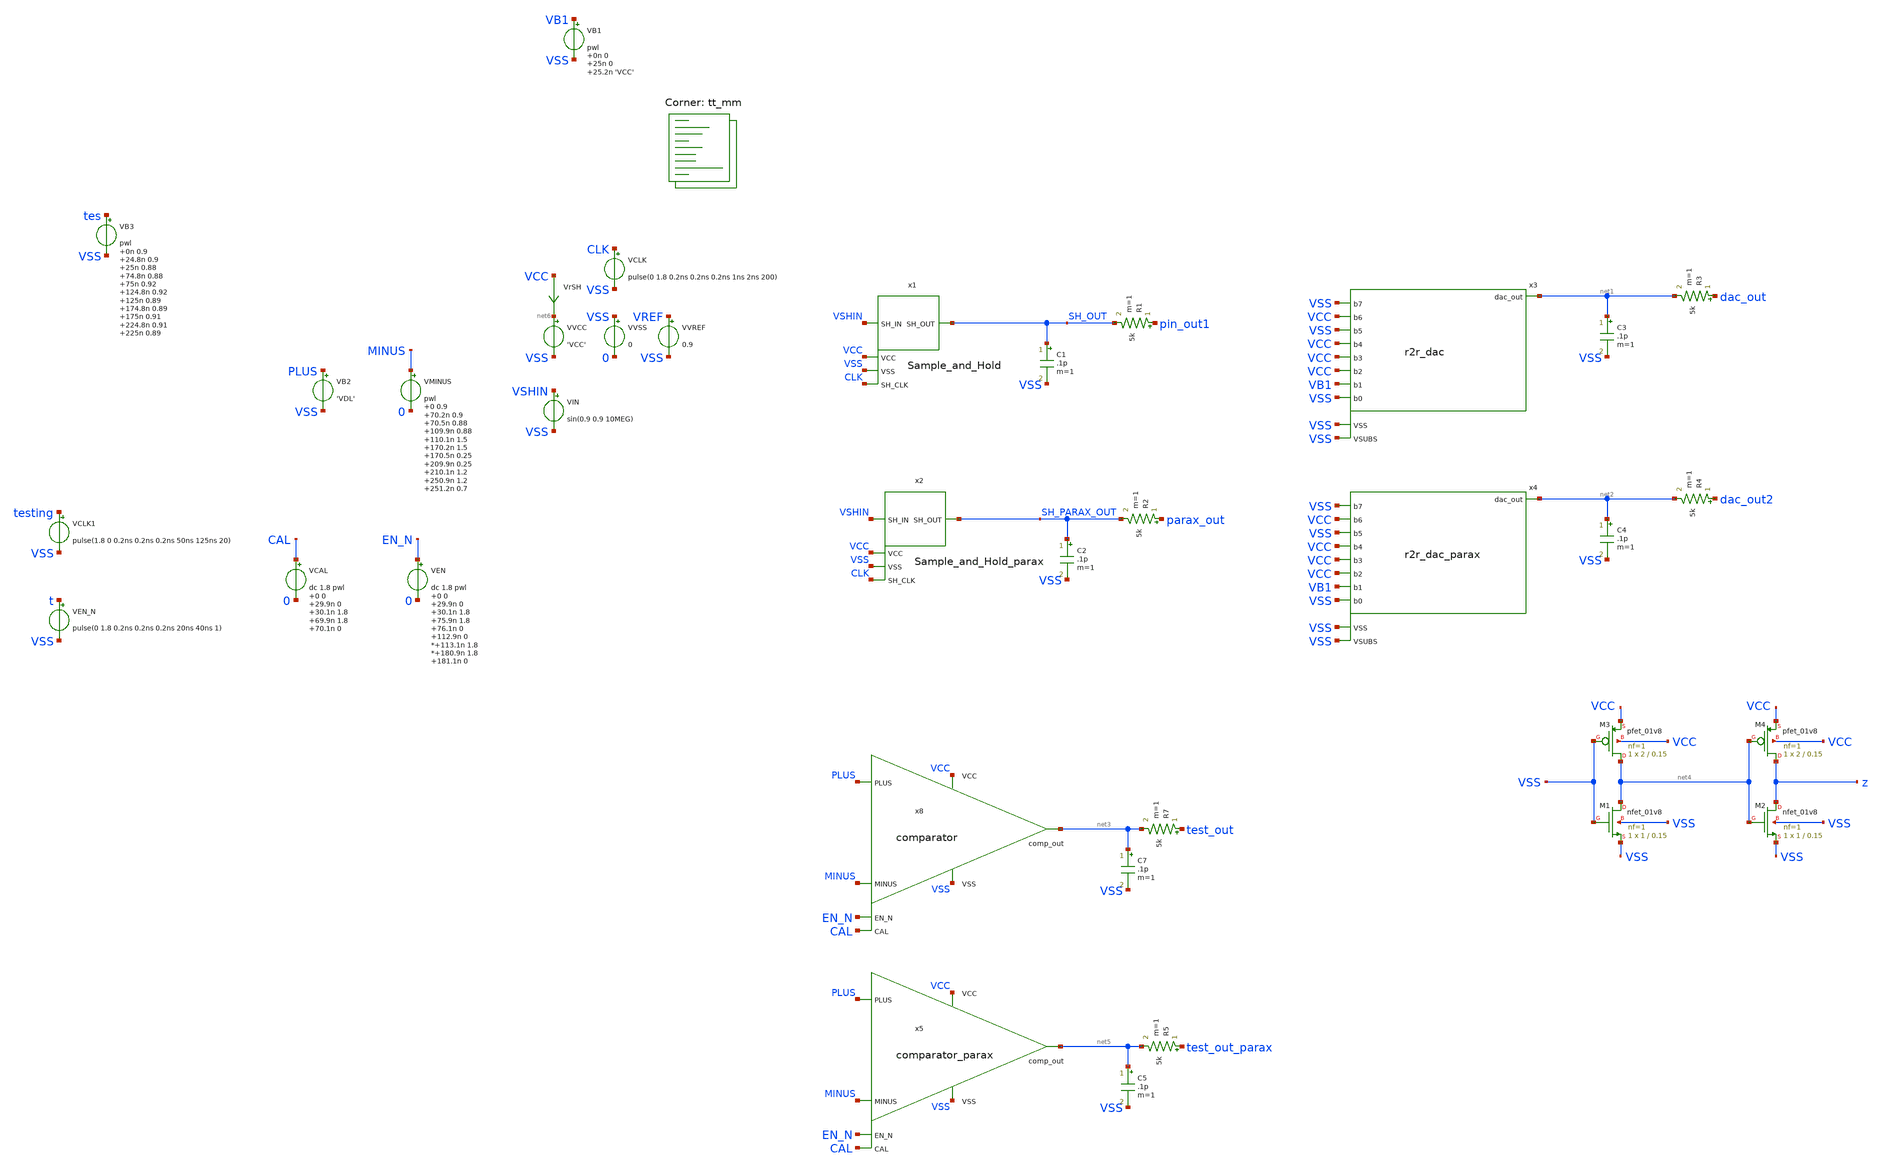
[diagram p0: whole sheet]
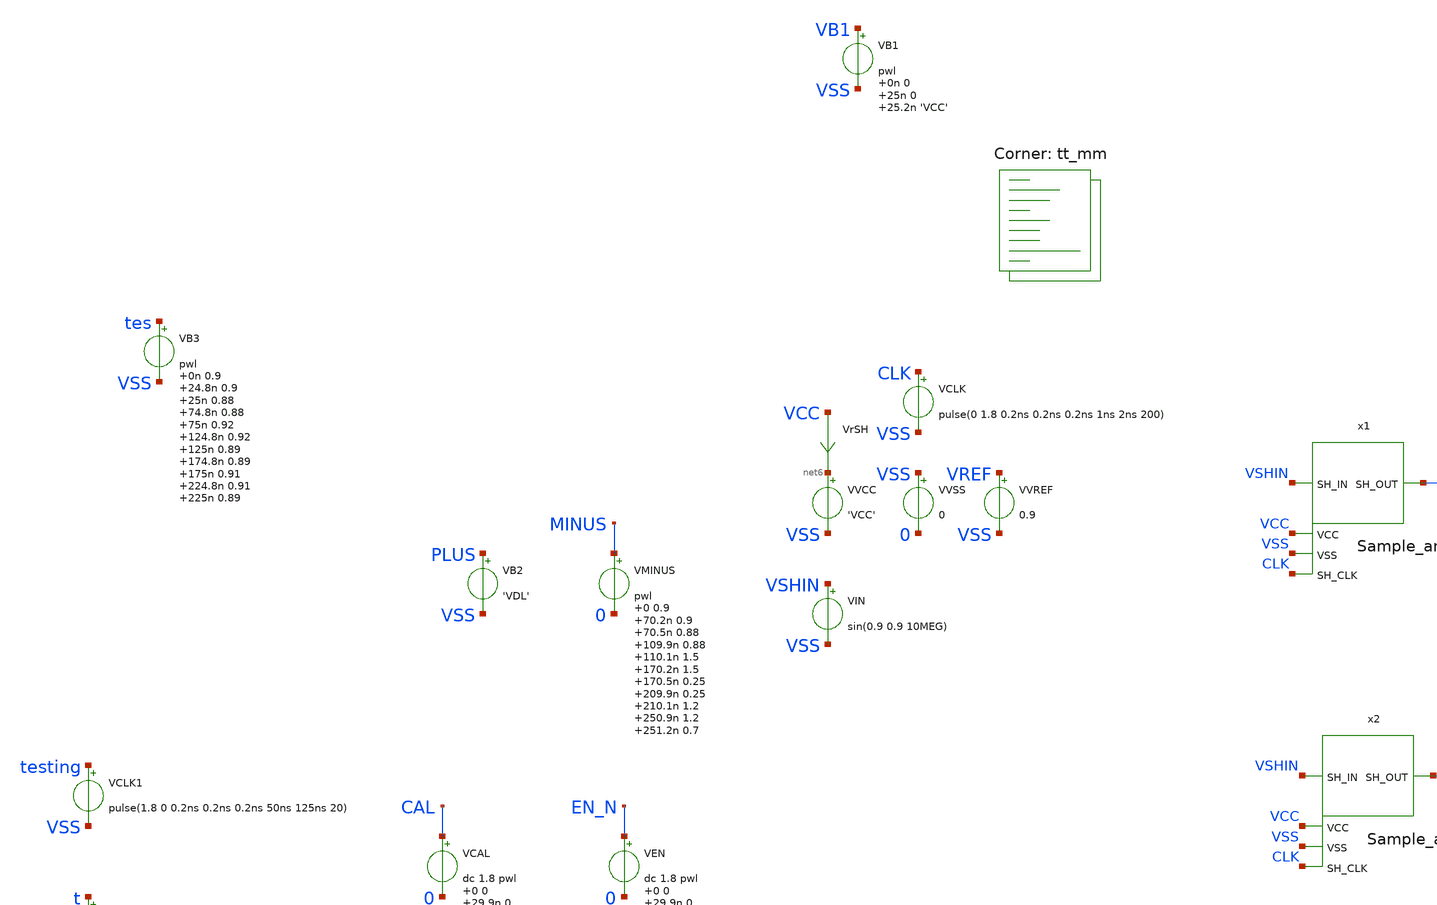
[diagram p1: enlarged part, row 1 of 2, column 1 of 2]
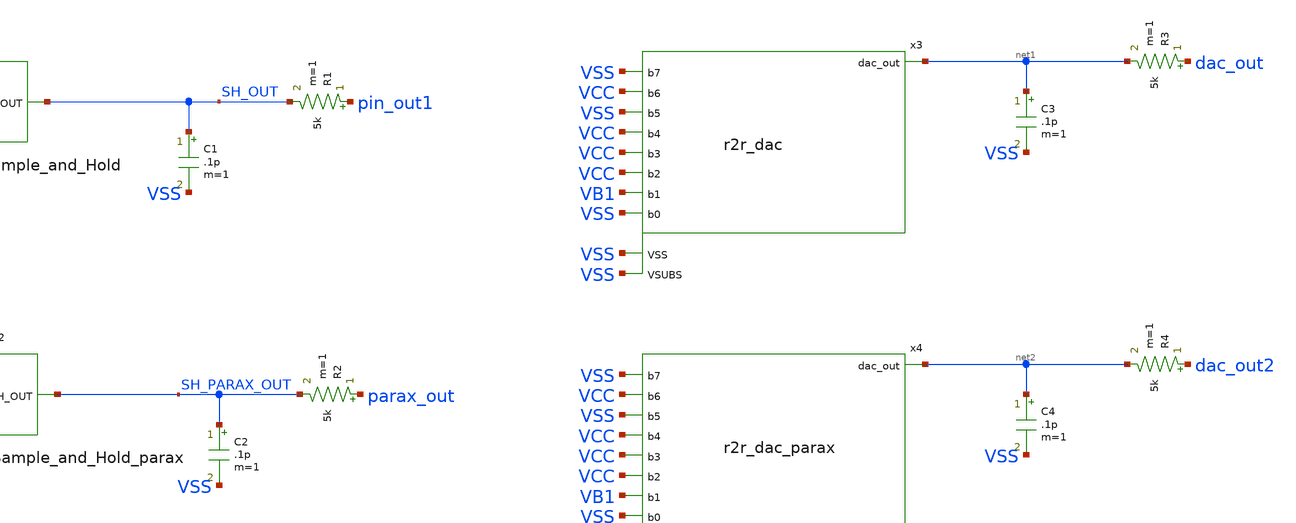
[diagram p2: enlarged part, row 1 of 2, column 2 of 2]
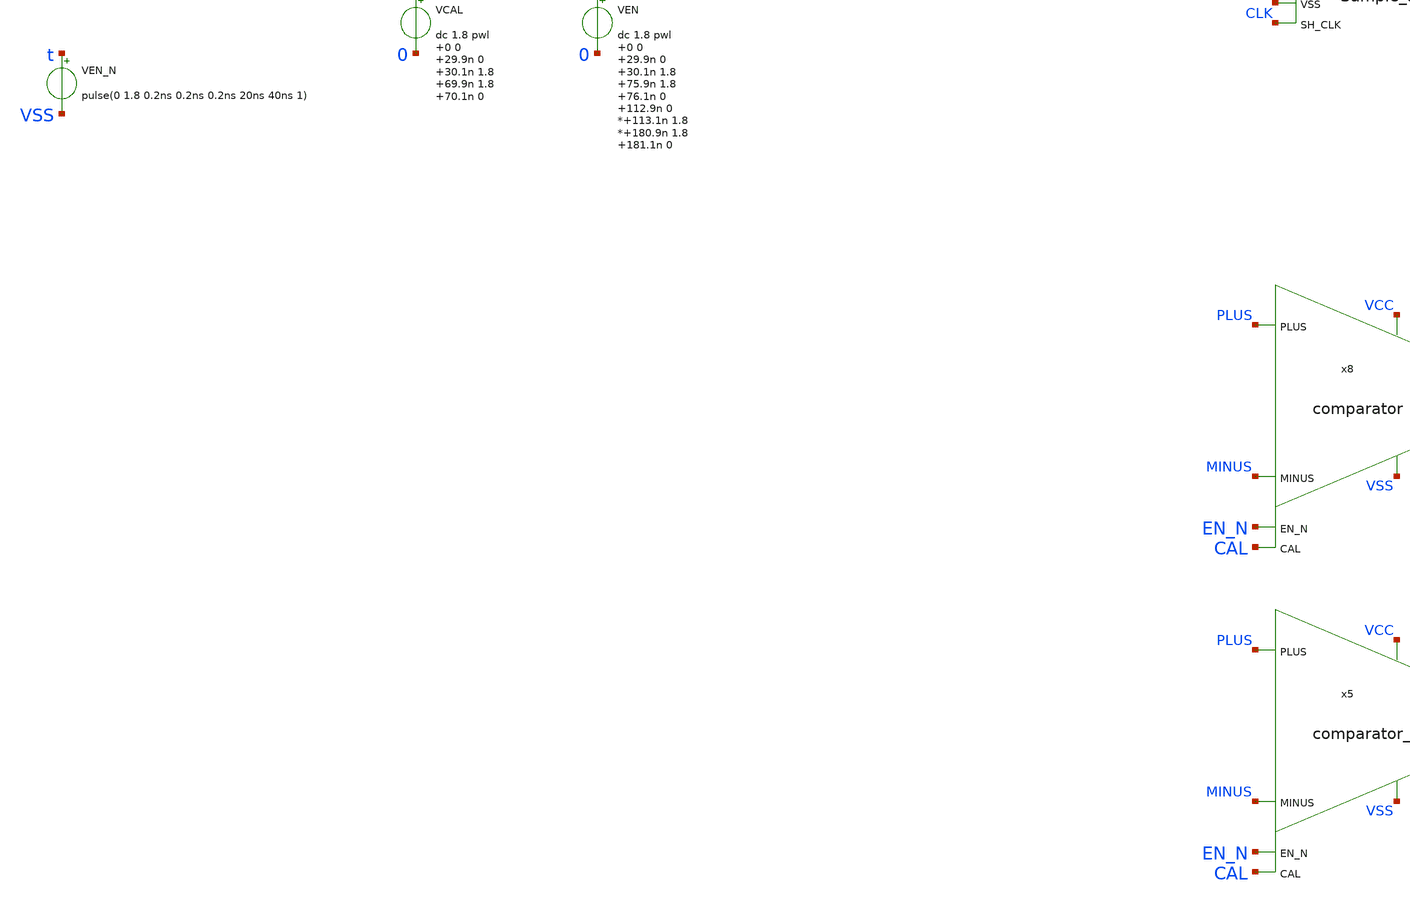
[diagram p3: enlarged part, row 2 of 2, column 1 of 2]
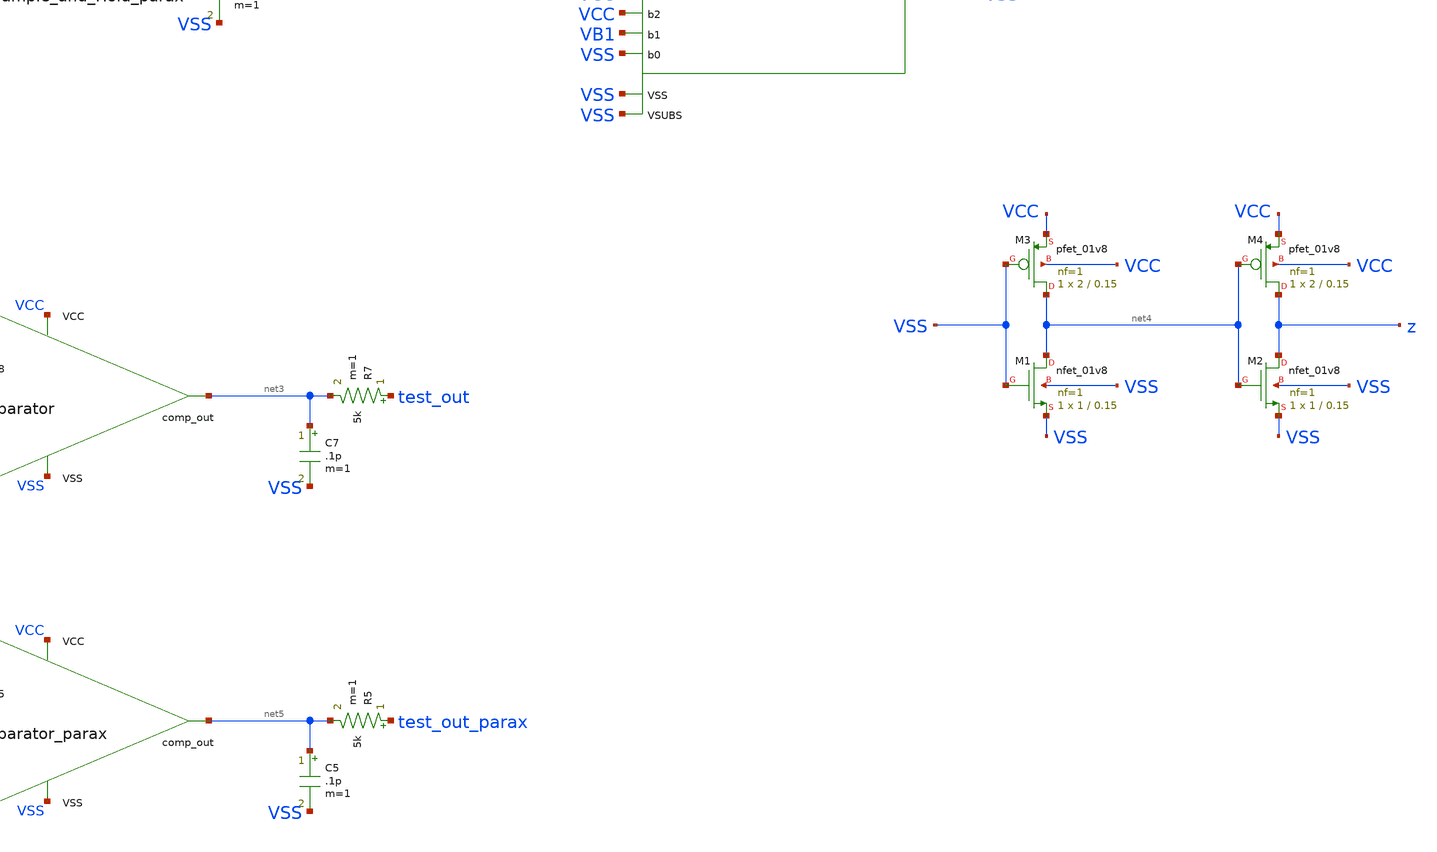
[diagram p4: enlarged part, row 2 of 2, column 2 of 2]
** sch_path: xschem/testbench.sch
**.subckt testbench
x1 SH_OUT VSHIN VSS VCC CLK Sample_and_Hold
VCLK CLK VSS pulse(0 1.8 0.2ns 0.2ns 0.2ns 1ns 2ns 200)
VVCC net6 VSS 'VCC'
VVSS VSS 0 0
VIN VSHIN VSS sin(0.9 0.9 10MEG)
VVREF VREF VSS 0.9
R1 pin_out1 SH_OUT 5k m=1
C1 SH_OUT VSS .1p m=1
VrSH VCC net6 0
.save i(vrsh)
x2 SH_PARAX_OUT VSHIN VSS VCC CLK Sample_and_Hold_parax
R2 parax_out SH_PARAX_OUT 5k m=1
C2 SH_PARAX_OUT VSS .1p m=1
x3 net1 VSS VB1 VCC VCC VSS VSS VCC VCC VSS VSS r2r_dac
VB1 VB1 VSS pwl 0n 0 25n 0 25.2n 'VCC'
R3 dac_out net1 5k m=1
C3 net1 VSS .1p m=1
x4 net2 VSS VB1 VCC VCC VSS VSS VCC VCC VSS VSS r2r_dac_parax
R4 dac_out2 net2 5k m=1
C4 net2 VSS .1p m=1
R7 test_out net3 5k m=1
C7 net3 VSS .1p m=1
x8 EN_N PLUS MINUS CAL net3 VCC VSS comparator
VB2 PLUS VSS 'VDL'
VB3 tes VSS pwl 0n 0.9 24.8n 0.9 25n 0.88 74.8n 0.88 75n 0.92 124.8n 0.92 125n 0.89 174.8n 0.89 175n
+ 0.91 224.8n 0.91 225n 0.89
VCLK1 testing VSS pulse(1.8 0 0.2ns 0.2ns 0.2ns 50ns 125ns 20)
XM1 net4 VSS VSS VSS sky130_fd_pr__nfet_01v8 L=0.15 W=1 nf=1 ad='int((nf+1)/2) * W/nf * 0.29' as='int((nf+2)/2) * W/nf * 0.29'
+ pd='2*int((nf+1)/2) * (W/nf + 0.29)' ps='2*int((nf+2)/2) * (W/nf + 0.29)' nrd='0.29 / W' nrs='0.29 / W'
+ sa=0 sb=0 sd=0 mult=1 m=1
XM2 z net4 VSS VSS sky130_fd_pr__nfet_01v8 L=0.15 W=1 nf=1 ad='int((nf+1)/2) * W/nf * 0.29' as='int((nf+2)/2) * W/nf * 0.29'
+ pd='2*int((nf+1)/2) * (W/nf + 0.29)' ps='2*int((nf+2)/2) * (W/nf + 0.29)' nrd='0.29 / W' nrs='0.29 / W'
+ sa=0 sb=0 sd=0 mult=1 m=1
XM3 net4 VSS VCC VCC sky130_fd_pr__pfet_01v8 L=0.15 W=2 nf=1 ad='int((nf+1)/2) * W/nf * 0.29' as='int((nf+2)/2) * W/nf * 0.29'
+ pd='2*int((nf+1)/2) * (W/nf + 0.29)' ps='2*int((nf+2)/2) * (W/nf + 0.29)' nrd='0.29 / W' nrs='0.29 / W'
+ sa=0 sb=0 sd=0 mult=1 m=1
XM4 z net4 VCC VCC sky130_fd_pr__pfet_01v8 L=0.15 W=2 nf=1 ad='int((nf+1)/2) * W/nf * 0.29' as='int((nf+2)/2) * W/nf * 0.29'
+ pd='2*int((nf+1)/2) * (W/nf + 0.29)' ps='2*int((nf+2)/2) * (W/nf + 0.29)' nrd='0.29 / W' nrs='0.29 / W'
+ sa=0 sb=0 sd=0 mult=1 m=1
VEN_N t VSS pulse(0 1.8 0.2ns 0.2ns 0.2ns 20ns 40ns 1)
VCAL CAL 0 dc 1.8 pwl 0 0 29.9n 0 30.1n 1.8 69.9n 1.8 70.1n 0
VEN EN_N 0 dc 1.8 pwl 0 0 29.9n 0 30.1n 1.8 75.9n 1.8 76.1n 0 112.9n 0
*+113.1n 1.8
*+180.9n 1.8 181.1n 0
VMINUS MINUS 0 pwl 0 0.9 70.2n 0.9 70.5n 0.88 109.9n 0.88 110.1n 1.5 170.2n 1.5 170.5n 0.25 209.9n
+ 0.25 210.1n 1.2 250.9n 1.2 251.2n 0.7 280.9n 0.7 281.1n 0.91 310.9n 0.91 311.1n 0.86
R5 test_out_parax net5 5k m=1
C5 net5 VSS .1p m=1
x5 EN_N PLUS MINUS CAL net5 VCC VSS comparator_parax
**** begin user architecture code
.lib $::SKYWATER_MODELS/sky130.lib.spice tt_mm


.option chgtol=4e-16 method=gear
.param VCCGAUSS = agauss(1.8, 0.05, 1)
.param VDLGAUSS = agauss(0.9, 0.23, 1)
.param TEMPGAUSS = agauss(40, 30, 1)
.param 'VCC' = 'VCCGAUSS'
.param 'VDL' = 0.9
.param 'DELTA' = 0.002
.param 'VREF' = 0.9
.option temp = 'TEMPGAUSS'
*.option temp = 27
*vvcc VCC 0 1.8
*vvss VSS 0 0
*vvref VREF 0 0.9
*vclk CLK pulse(1ns 1ns 1ns 5ns 10ns 25)
*vvshin VSHIN sin(0.9 0.9 10MEG)


.control
  setseed  8
  reset
  save all
  savecurrents
  op
  write testbench.raw
  reset
  set appendwrite
  *repeat 10
    save all
    tran 0.1n 320n uic
    write testbench.raw
    set appendwrite
    reset
  *end
  quit 0
.endc

**** end user architecture code
**.ends
.end
